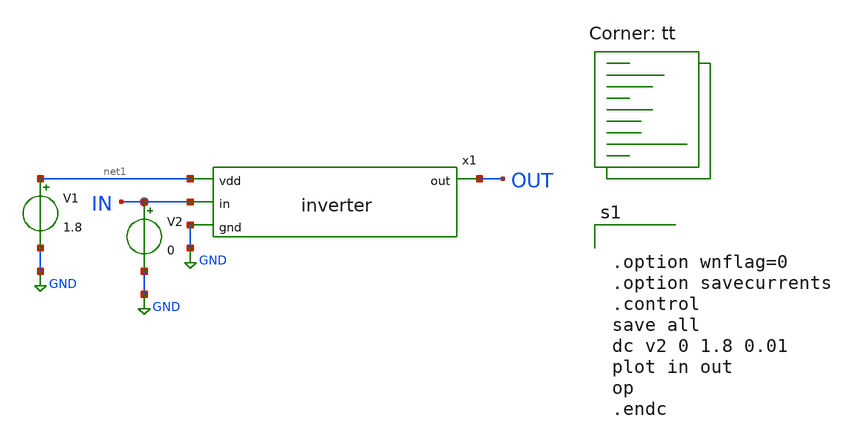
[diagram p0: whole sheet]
** sch_path: xschem/inverter_tb.sch
**.subckt inverter_tb
x1 net1 OUT IN GND inverter
V1 net1 GND 1.8
V2 IN GND 0
**** begin user architecture code
.lib $::SKYWATER_MODELS/sky130.lib.spice tt


.option wnflag=0
.option savecurrents
.control
save all
dc v2 0 1.8 0.01
plot in out
op
.endc


**** end user architecture code
**.ends

* expanding   symbol:  /home/mtfirmansyah/ic_projects/inverter/xschem/inverter.sym # of pins=4
** sym_path: xschem/inverter.sym
** sch_path: xschem/inverter.sch
.subckt inverter vdd out in gnd
*.ipin in
*.ipin vdd
*.opin out
*.ipin gnd
XM1 out in gnd gnd sky130_fd_pr__nfet_01v8 L=0.15 W=1 nf=1 ad='int((nf+1)/2) * W/nf * 0.29' as='int((nf+2)/2) * W/nf * 0.29'
+ pd='2*int((nf+1)/2) * (W/nf + 0.29)' ps='2*int((nf+2)/2) * (W/nf + 0.29)' nrd='0.29 / W' nrs='0.29 / W'
+ sa=0 sb=0 sd=0 mult=1 m=1
XM2 out in vdd vdd sky130_fd_pr__pfet_01v8 L=0.15 W=1 nf=1 ad='int((nf+1)/2) * W/nf * 0.29' as='int((nf+2)/2) * W/nf * 0.29'
+ pd='2*int((nf+1)/2) * (W/nf + 0.29)' ps='2*int((nf+2)/2) * (W/nf + 0.29)' nrd='0.29 / W' nrs='0.29 / W'
+ sa=0 sb=0 sd=0 mult=1 m=1
.ends

.GLOBAL GND
.end
